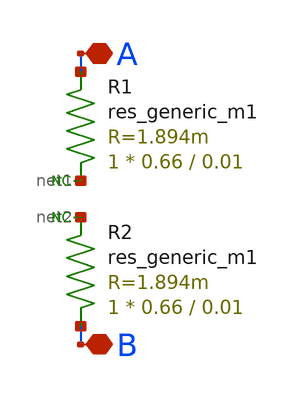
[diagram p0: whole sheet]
** sch_path: common/tk_em1o.sch
* Copyright 2023 David Mitchell Bailey
* Licensed under the Apache License, Version 2.0 (the "License");
* you may not use this file except in compliance with the License.
* You may obtain a copy of the License at
* https://www.apache.org/licenses/LICENSE-2.0
* Unless required by applicable law or agreed to in writing, software
* distributed under the License is distributed on an "AS IS" BASIS,
* WITHOUT WARRANTIES OR CONDITIONS OF ANY KIND, either express or implied.
* See the License for the specific language governing permissions and
* limitations under the License.
**.subckt tk_em1o A B
*.iopin A
*.iopin B
R1 net1 A sky130_fd_pr__res_generic_m1 W=0.66 L=0.01 m=1
R2 B net2 sky130_fd_pr__res_generic_m1 W=0.66 L=0.01 m=1
* noconn #net1
* noconn #net2
**.ends
.end
